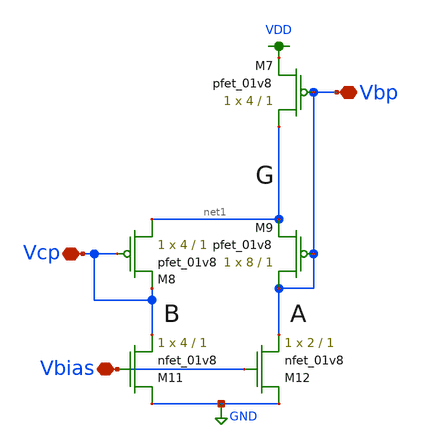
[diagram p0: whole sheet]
** sch_path: schematics/new_cascode.sch
**.subckt new_cascode Vcp Vbp Vbias
*.iopin Vcp
*.iopin Vbp
*.iopin Vbias
XM9 Vbp Vbp net1 VDD sky130_fd_pr__pfet_01v8 L=1 W=8 nf=1 ad='int((nf+1)/2) * W/nf * 0.29' as='int((nf+2)/2) * W/nf * 0.29'
+ pd='2*int((nf+1)/2) * (W/nf + 0.29)' ps='2*int((nf+2)/2) * (W/nf + 0.29)' nrd='0.29 / W' nrs='0.29 / W'
+ sa=0 sb=0 sd=0 mult=1 m=1
XM11 GND Vbias Vcp GND sky130_fd_pr__nfet_01v8 L=1 W=4 nf=1 ad='int((nf+1)/2) * W/nf * 0.29' as='int((nf+2)/2) * W/nf * 0.29'
+ pd='2*int((nf+1)/2) * (W/nf + 0.29)' ps='2*int((nf+2)/2) * (W/nf + 0.29)' nrd='0.29 / W' nrs='0.29 / W'
+ sa=0 sb=0 sd=0 mult=1 m=1
XM8 net1 Vcp Vcp VDD sky130_fd_pr__pfet_01v8 L=1 W=4 nf=1 ad='int((nf+1)/2) * W/nf * 0.29' as='int((nf+2)/2) * W/nf * 0.29'
+ pd='2*int((nf+1)/2) * (W/nf + 0.29)' ps='2*int((nf+2)/2) * (W/nf + 0.29)' nrd='0.29 / W' nrs='0.29 / W'
+ sa=0 sb=0 sd=0 mult=1 m=1
XM12 GND Vbias Vbp GND sky130_fd_pr__nfet_01v8 L=1 W=2 nf=1 ad='int((nf+1)/2) * W/nf * 0.29' as='int((nf+2)/2) * W/nf * 0.29'
+ pd='2*int((nf+1)/2) * (W/nf + 0.29)' ps='2*int((nf+2)/2) * (W/nf + 0.29)' nrd='0.29 / W' nrs='0.29 / W'
+ sa=0 sb=0 sd=0 mult=1 m=1
XM7 net1 Vbp VDD VDD sky130_fd_pr__pfet_01v8 L=1 W=4 nf=1 ad='int((nf+1)/2) * W/nf * 0.29' as='int((nf+2)/2) * W/nf * 0.29'
+ pd='2*int((nf+1)/2) * (W/nf + 0.29)' ps='2*int((nf+2)/2) * (W/nf + 0.29)' nrd='0.29 / W' nrs='0.29 / W'
+ sa=0 sb=0 sd=0 mult=1 m=1
**.ends
.GLOBAL GND
.GLOBAL VDD
.end
